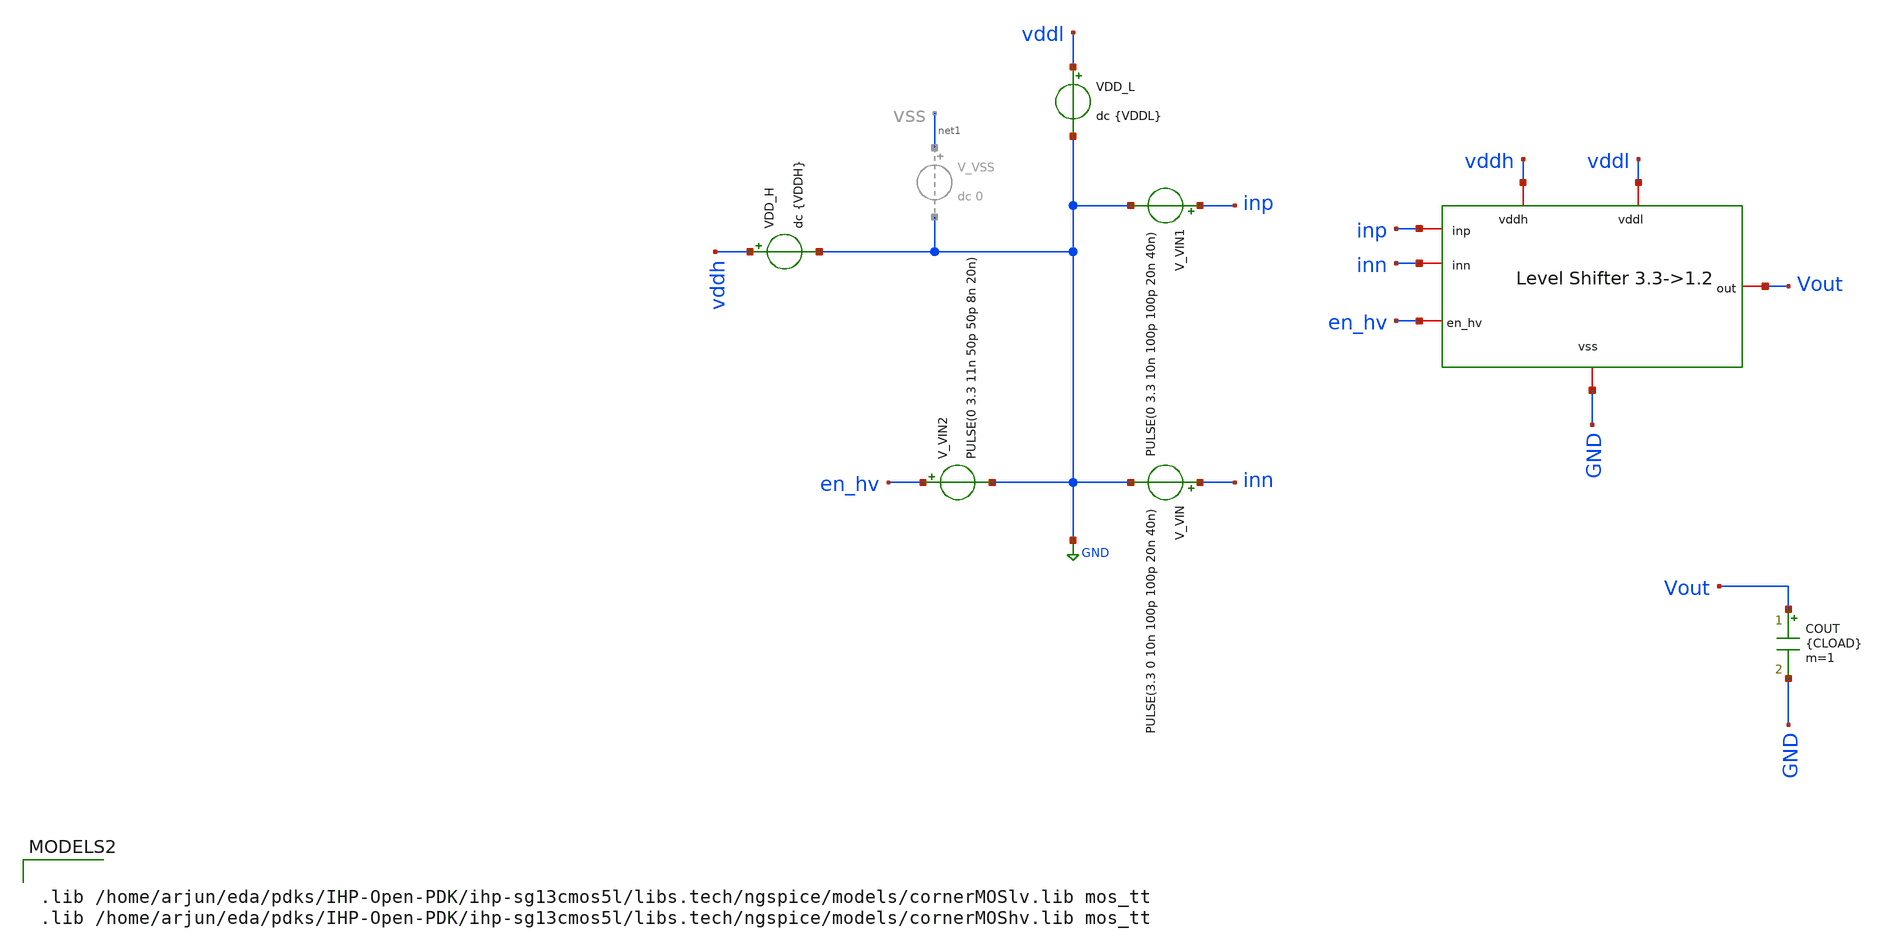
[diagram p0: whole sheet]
** sch_path: circuit_files/sar_adc_test/xschem/LS_h2l_tb.sch
**.subckt LS_h2l_tb
V_VIN inn GND PULSE(3.3 0 10n 100p 100p 20n 40n)
VDD_L vddl GND dc {VDDL}
COUT Vout GND {CLOAD} m=1
V_VIN1 inp GND PULSE(0 3.3 10n 100p 100p 20n 40n)
V_VIN2 en_hv GND PULSE(0 3.3 11n 50p 50p 8n 20n)
x1 GND vddl vddh Vout inp inn en_hv level_shifter_3v3_to_1v2
VDD_H vddh GND dc {VDDH}
**** begin user architecture code

.lib /home/arjun/eda/pdks/IHP-Open-PDK/ihp-sg13cmos5l/libs.tech/ngspice/models/cornerMOSlv.lib mos_tt
.lib /home/arjun/eda/pdks/IHP-Open-PDK/ihp-sg13cmos5l/libs.tech/ngspice/models/cornerMOShv.lib mos_tt




.param VDDL=1.2
.param VDDH=3.3

.param CLOAD=5f
.save v(inp)
.save v(inn)
.save v(en_hv)

.save v(vddl)
.save v(vddh)

.save v(x1.enb)
.save v(x1.gatep)
.save v(x1.gaten)

.save v(x1.q)
.save v(x1.qb)

.save v(x1.xp)
.save v(x1.xn)

.save v(x1.hbuf)
.save v(x1.hbuf2)
.save v(x1.lvbuf)

.save v(Vout)

.save i(VDD_L)
.save i(VDD_H)

.options savecurrents
.options reltol=1e-4
.options abstol=1e-12
.options vntol=1e-6
.options method=gear
.options maxord=2
.options plotwinsize=0
.options itl4=500




.control

set noaskquit

reset

alter COUT 5f
alter VDD_L 1.2

alter @V_VIN1[pulse] [ 0 3.3 10n 100p 100p 20n 40n ]
alter @V_VIN[pulse]  [ 3.3 0 10n 100p 100p 20n 40n ]

* Turn receiver on at 11ns and leave it on
alter @V_VIN2[pulse] [ 0 3.3 11n 50p 50p 100n 200n ]

tran 2p 70n 0 5p

meas tran c20 FIND v(Vout) AT=20n
meas tran c25 FIND v(Vout) AT=25n
meas tran c30 FIND v(Vout) AT=30n
meas tran c35 FIND v(Vout) AT=35n
meas tran c40 FIND v(Vout) AT=40n
meas tran c45 FIND v(Vout) AT=45n
meas tran c55 FIND v(Vout) AT=55n
meas tran c65 FIND v(Vout) AT=65n

print c20
print c25
print c30
print c35
print c40
print c45
print c55
print c65

plot v(inp) v(inn) v(en_hv)

plot v(x1.q) v(x1.qb)

plot v(x1.xp) v(x1.xn)

plot v(x1.yp) v(x1.yn)

plot v(x1.hbuf) v(x1.hbuf2)

plot v(x1.lvbuf) v(Vout)

.endc


**** end user architecture code
**.ends
.GLOBAL GND
.end
